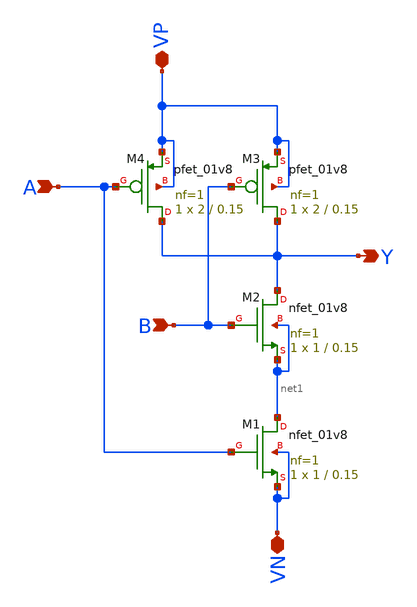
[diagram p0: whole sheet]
** sch_path: projects/nand/xschem_ngspice/nand.sch
**.subckt nand A B Y VP VN
*.ipin A
*.ipin B
*.opin Y
*.iopin VP
*.iopin VN
XM1 net1 A VN VN sky130_fd_pr__nfet_01v8 L=0.15 W=1 nf=1 ad='int((nf+1)/2) * W/nf * 0.29' as='int((nf+2)/2) * W/nf * 0.29'
+ pd='2*int((nf+1)/2) * (W/nf + 0.29)' ps='2*int((nf+2)/2) * (W/nf + 0.29)' nrd='0.29 / W' nrs='0.29 / W'
+ sa=0 sb=0 sd=0 mult=1 m=1
XM2 Y B net1 net1 sky130_fd_pr__nfet_01v8 L=0.15 W=1 nf=1 ad='int((nf+1)/2) * W/nf * 0.29' as='int((nf+2)/2) * W/nf * 0.29'
+ pd='2*int((nf+1)/2) * (W/nf + 0.29)' ps='2*int((nf+2)/2) * (W/nf + 0.29)' nrd='0.29 / W' nrs='0.29 / W'
+ sa=0 sb=0 sd=0 mult=1 m=1
XM3 Y B VP VP sky130_fd_pr__pfet_01v8 L=0.15 W=2 nf=1 ad='int((nf+1)/2) * W/nf * 0.29' as='int((nf+2)/2) * W/nf * 0.29'
+ pd='2*int((nf+1)/2) * (W/nf + 0.29)' ps='2*int((nf+2)/2) * (W/nf + 0.29)' nrd='0.29 / W' nrs='0.29 / W'
+ sa=0 sb=0 sd=0 mult=1 m=1
XM4 Y A VP VP sky130_fd_pr__pfet_01v8 L=0.15 W=2 nf=1 ad='int((nf+1)/2) * W/nf * 0.29' as='int((nf+2)/2) * W/nf * 0.29'
+ pd='2*int((nf+1)/2) * (W/nf + 0.29)' ps='2*int((nf+2)/2) * (W/nf + 0.29)' nrd='0.29 / W' nrs='0.29 / W'
+ sa=0 sb=0 sd=0 mult=1 m=1
**.ends
.end
